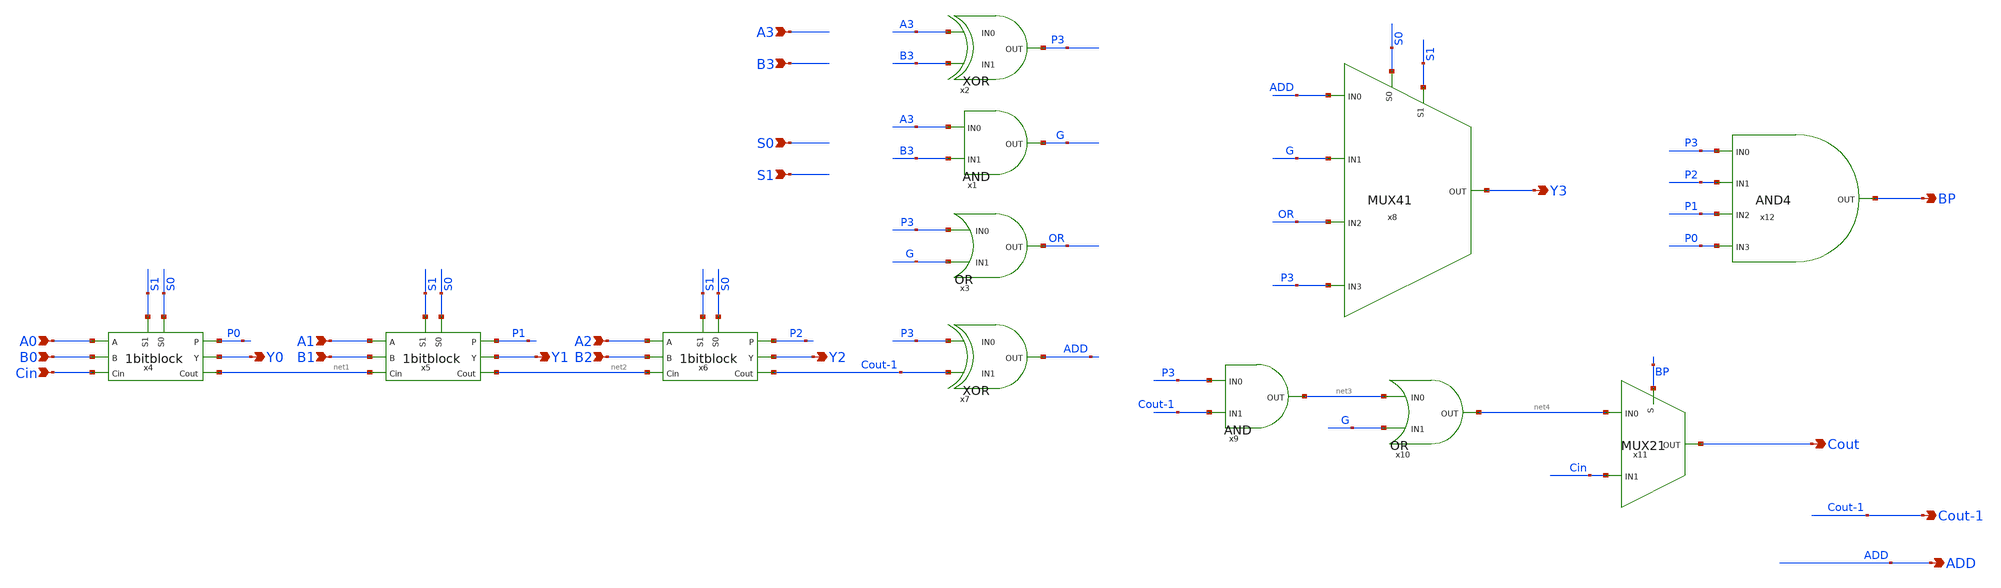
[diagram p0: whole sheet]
** sch_path: schematics/add/4bitblock_LAST.sch
**.subckt 4bitblock_LAST A0 B0 Cin Y0 A1 B1 A2 B2 Y1 Y2 A3 B3 S0 S1 Y3 Cout BP ADD Cout-1
*.ipin A0
*.ipin B0
*.ipin Cin
*.opin Y0
*.ipin A1
*.ipin B1
*.ipin A2
*.ipin B2
*.opin Y1
*.opin Y2
*.ipin A3
*.ipin B3
*.ipin S0
*.ipin S1
*.opin Y3
*.opin Cout
*.opin BP
*.opin ADD
*.opin Cout-1
x4 P0 A0 B0 Cin S0 S1 Y0 net1 1bitblock
x5 P1 A1 B1 net1 S0 S1 Y1 net2 1bitblock
x6 P2 A2 B2 net2 S0 S1 Y2 Cout-1 1bitblock
x1 A3 G B3 AND
x2 A3 B3 P3 XOR
x3 P3 G OR OR
x7 P3 Cout-1 ADD XOR
x8 S0 ADD S1 G Y3 OR P3 MUX41
x9 P3 net3 Cout-1 AND
x10 net3 G net4 OR
x11 net4 BP Cout Cin MUX21
x12 BP P3 P2 P1 P0 AND4
**.ends
.end
